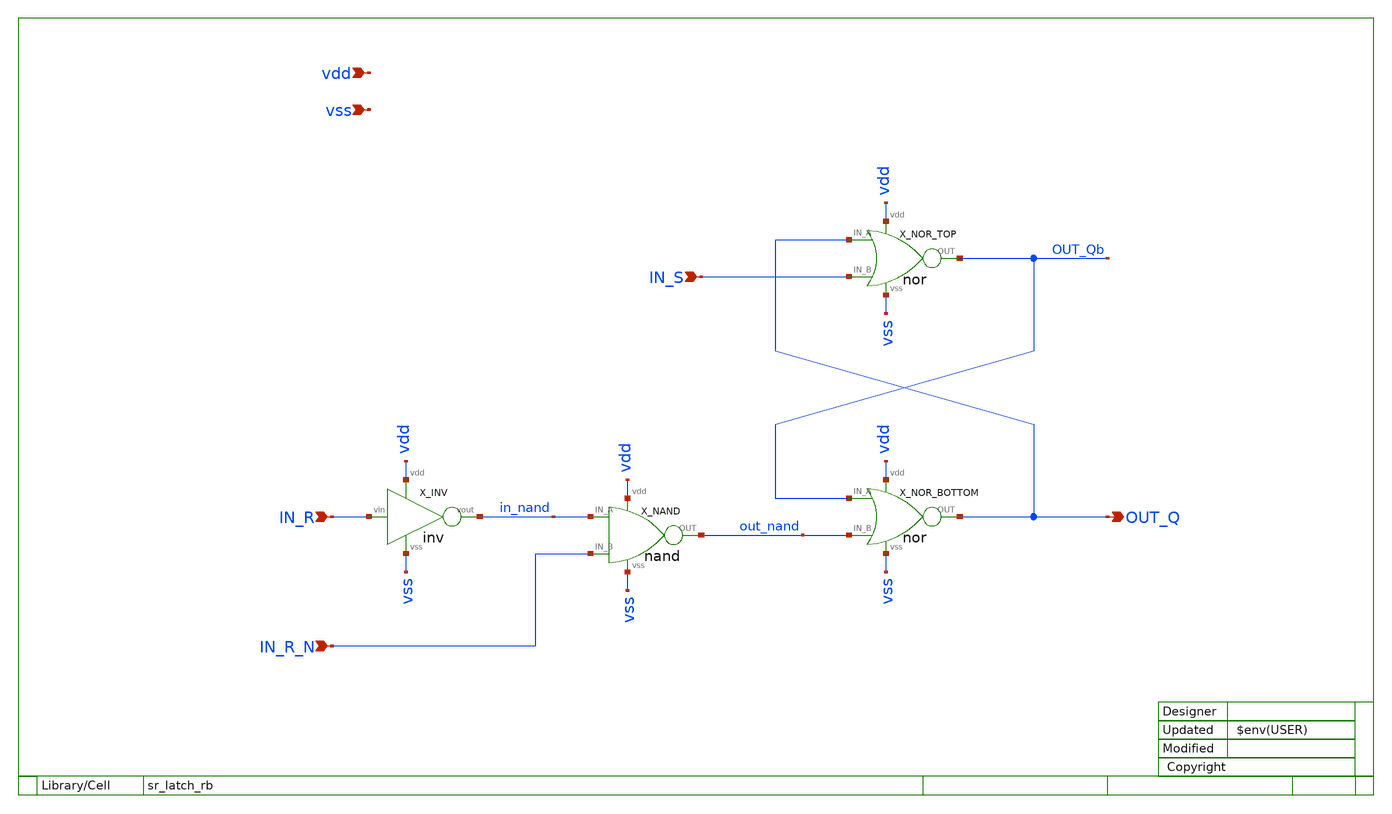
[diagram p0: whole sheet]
** sch_path: xsch/ip/logic/sr_latch_rb/sr_latch_rb.sch
**.subckt sr_latch_rb IN_R OUT_Q IN_S vdd vss IN_R_N
*.ipin IN_R
*.opin OUT_Q
*.ipin IN_S
*.ipin vdd
*.ipin vss
*.ipin IN_R_N
X_NOR_TOP OUT_Q IN_S OUT_Qb vdd vss nor
X_NOR_BOTTOM OUT_Qb out_nand OUT_Q vdd vss nor
X_NAND in_nand IN_R_N out_nand vdd vss nand
X_INV IN_R in_nand vdd vss inv
**.ends
.end
